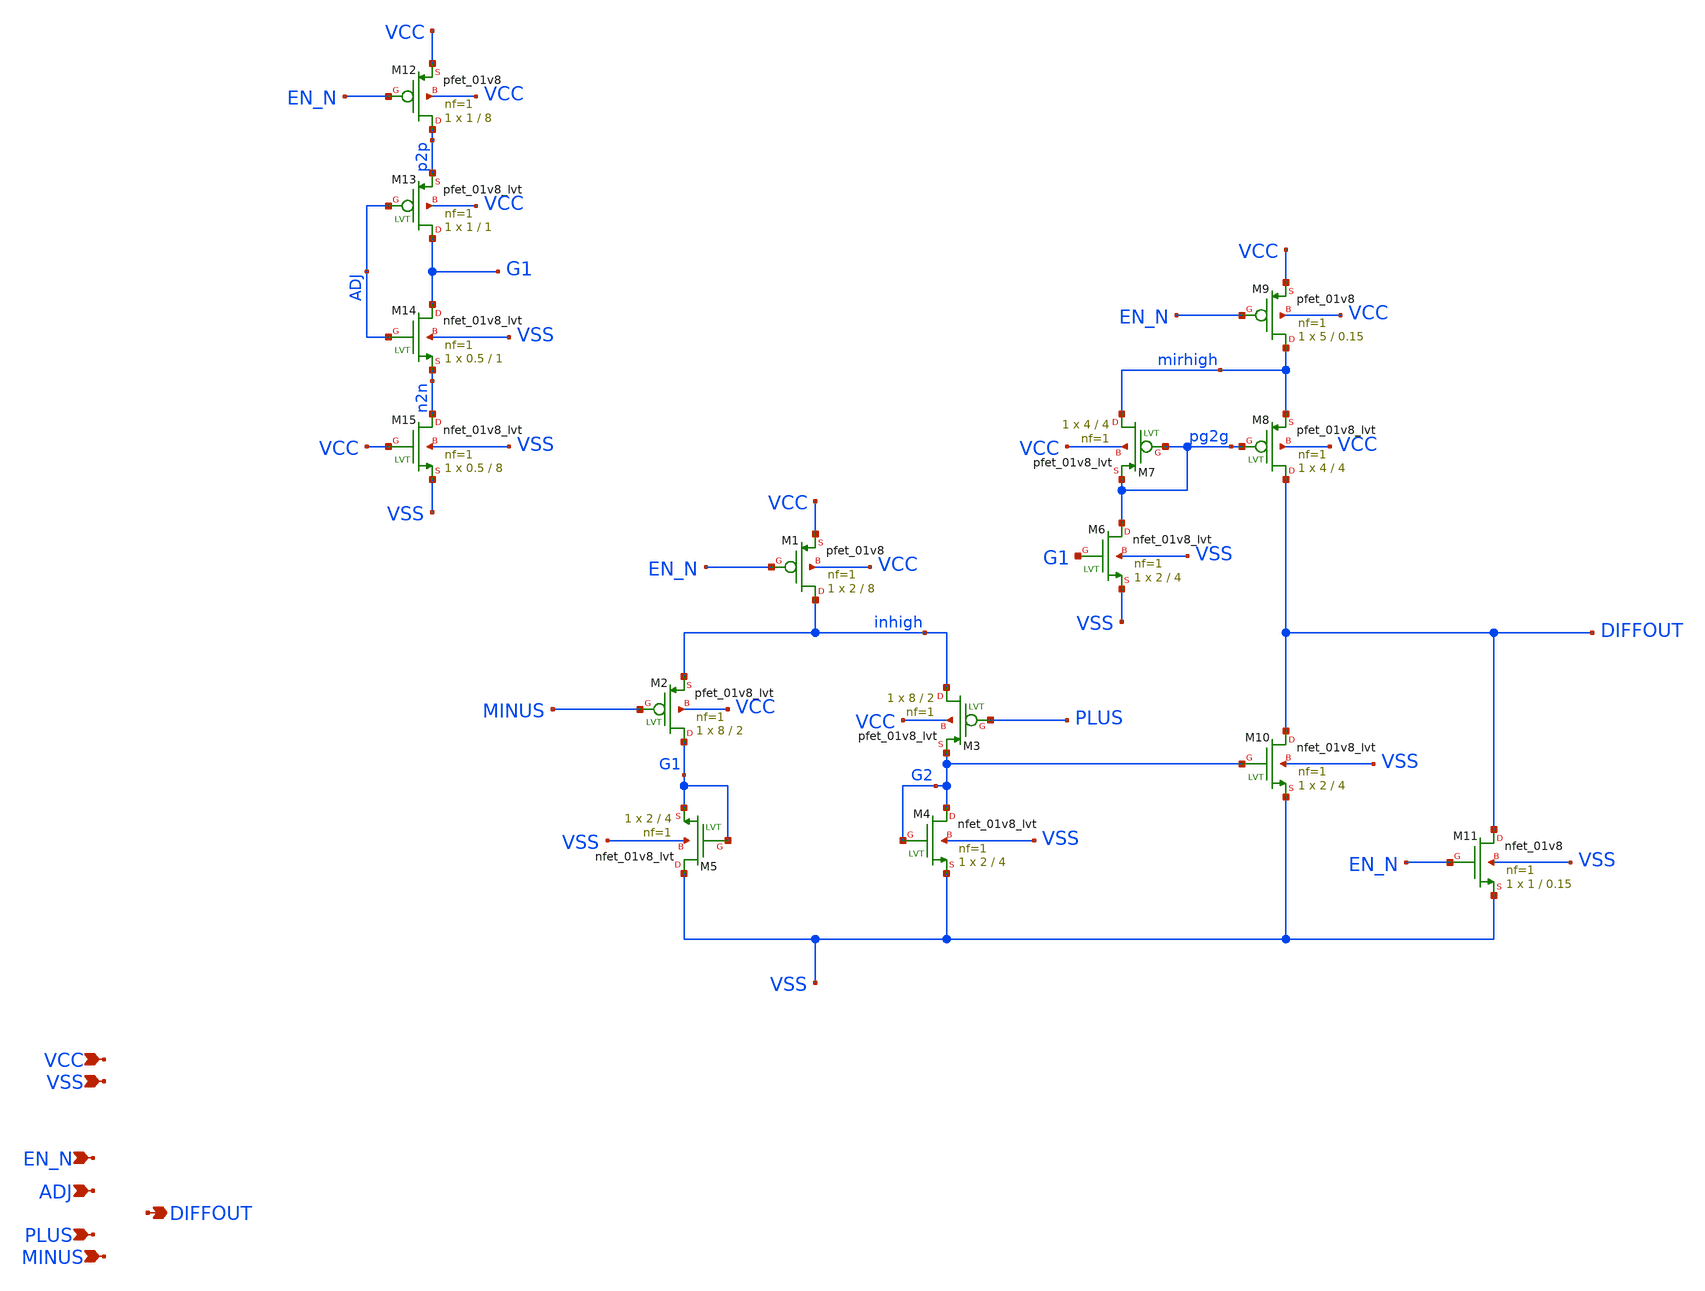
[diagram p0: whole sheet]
** sch_path: xschem/comparator_stefan.sch
**.subckt comparator_stefan PLUS MINUS VCC VSS EN_N ADJ DIFFOUT
*.ipin PLUS
*.ipin MINUS
*.ipin VCC
*.ipin VSS
*.ipin EN_N
*.ipin ADJ
*.opin DIFFOUT
XM1 inhigh EN_N VCC VCC sky130_fd_pr__pfet_01v8 L=8 W=2 nf=1 ad='int((nf+1)/2) * W/nf * 0.29' as='int((nf+2)/2) * W/nf * 0.29'
+ pd='2*int((nf+1)/2) * (W/nf + 0.29)' ps='2*int((nf+2)/2) * (W/nf + 0.29)' nrd='0.29 / W' nrs='0.29 / W'
+ sa=0 sb=0 sd=0 mult=1 m=1
XM2 G1 MINUS inhigh VCC sky130_fd_pr__pfet_01v8_lvt L=2 W=8 nf=1 ad='int((nf+1)/2) * W/nf * 0.29' as='int((nf+2)/2) * W/nf * 0.29'
+ pd='2*int((nf+1)/2) * (W/nf + 0.29)' ps='2*int((nf+2)/2) * (W/nf + 0.29)' nrd='0.29 / W' nrs='0.29 / W'
+ sa=0 sb=0 sd=0 mult=1 m=1
XM3 inhigh PLUS G2 VCC sky130_fd_pr__pfet_01v8_lvt L=2 W=8 nf=1 ad='int((nf+1)/2) * W/nf * 0.29' as='int((nf+2)/2) * W/nf * 0.29'
+ pd='2*int((nf+1)/2) * (W/nf + 0.29)' ps='2*int((nf+2)/2) * (W/nf + 0.29)' nrd='0.29 / W' nrs='0.29 / W'
+ sa=0 sb=0 sd=0 mult=1 m=1
XM4 G2 G2 VSS VSS sky130_fd_pr__nfet_01v8_lvt L=4 W=2 nf=1 ad='int((nf+1)/2) * W/nf * 0.29' as='int((nf+2)/2) * W/nf * 0.29'
+ pd='2*int((nf+1)/2) * (W/nf + 0.29)' ps='2*int((nf+2)/2) * (W/nf + 0.29)' nrd='0.29 / W' nrs='0.29 / W'
+ sa=0 sb=0 sd=0 mult=1 m=1
XM5 VSS G1 G1 VSS sky130_fd_pr__nfet_01v8_lvt L=4 W=2 nf=1 ad='int((nf+1)/2) * W/nf * 0.29' as='int((nf+2)/2) * W/nf * 0.29'
+ pd='2*int((nf+1)/2) * (W/nf + 0.29)' ps='2*int((nf+2)/2) * (W/nf + 0.29)' nrd='0.29 / W' nrs='0.29 / W'
+ sa=0 sb=0 sd=0 mult=1 m=1
XM6 pg2g G1 VSS VSS sky130_fd_pr__nfet_01v8_lvt L=4 W=2 nf=1 ad='int((nf+1)/2) * W/nf * 0.29' as='int((nf+2)/2) * W/nf * 0.29'
+ pd='2*int((nf+1)/2) * (W/nf + 0.29)' ps='2*int((nf+2)/2) * (W/nf + 0.29)' nrd='0.29 / W' nrs='0.29 / W'
+ sa=0 sb=0 sd=0 mult=1 m=1
XM7 mirhigh pg2g pg2g VCC sky130_fd_pr__pfet_01v8_lvt L=4 W=4 nf=1 ad='int((nf+1)/2) * W/nf * 0.29' as='int((nf+2)/2) * W/nf * 0.29'
+ pd='2*int((nf+1)/2) * (W/nf + 0.29)' ps='2*int((nf+2)/2) * (W/nf + 0.29)' nrd='0.29 / W' nrs='0.29 / W'
+ sa=0 sb=0 sd=0 mult=1 m=1
XM8 DIFFOUT pg2g mirhigh VCC sky130_fd_pr__pfet_01v8_lvt L=4 W=4 nf=1 ad='int((nf+1)/2) * W/nf * 0.29'
+ as='int((nf+2)/2) * W/nf * 0.29' pd='2*int((nf+1)/2) * (W/nf + 0.29)' ps='2*int((nf+2)/2) * (W/nf + 0.29)'
+ nrd='0.29 / W' nrs='0.29 / W' sa=0 sb=0 sd=0 mult=1 m=1
XM9 mirhigh EN_N VCC VCC sky130_fd_pr__pfet_01v8 L=0.15 W=5 nf=1 ad='int((nf+1)/2) * W/nf * 0.29' as='int((nf+2)/2) * W/nf * 0.29'
+ pd='2*int((nf+1)/2) * (W/nf + 0.29)' ps='2*int((nf+2)/2) * (W/nf + 0.29)' nrd='0.29 / W' nrs='0.29 / W'
+ sa=0 sb=0 sd=0 mult=1 m=1
XM10 DIFFOUT G2 VSS VSS sky130_fd_pr__nfet_01v8_lvt L=4 W=2 nf=1 ad='int((nf+1)/2) * W/nf * 0.29' as='int((nf+2)/2) * W/nf * 0.29'
+ pd='2*int((nf+1)/2) * (W/nf + 0.29)' ps='2*int((nf+2)/2) * (W/nf + 0.29)' nrd='0.29 / W' nrs='0.29 / W'
+ sa=0 sb=0 sd=0 mult=1 m=1
XM11 DIFFOUT EN_N VSS VSS sky130_fd_pr__nfet_01v8 L=0.15 W=1 nf=1 ad='int((nf+1)/2) * W/nf * 0.29' as='int((nf+2)/2) * W/nf * 0.29'
+ pd='2*int((nf+1)/2) * (W/nf + 0.29)' ps='2*int((nf+2)/2) * (W/nf + 0.29)' nrd='0.29 / W' nrs='0.29 / W'
+ sa=0 sb=0 sd=0 mult=1 m=1
XM12 p2p EN_N VCC VCC sky130_fd_pr__pfet_01v8 L=8 W=1 nf=1 ad='int((nf+1)/2) * W/nf * 0.29' as='int((nf+2)/2) * W/nf * 0.29'
+ pd='2*int((nf+1)/2) * (W/nf + 0.29)' ps='2*int((nf+2)/2) * (W/nf + 0.29)' nrd='0.29 / W' nrs='0.29 / W'
+ sa=0 sb=0 sd=0 mult=1 m=1
XM13 G1 ADJ p2p VCC sky130_fd_pr__pfet_01v8_lvt L=1 W=1 nf=1 ad='int((nf+1)/2) * W/nf * 0.29' as='int((nf+2)/2) * W/nf * 0.29'
+ pd='2*int((nf+1)/2) * (W/nf + 0.29)' ps='2*int((nf+2)/2) * (W/nf + 0.29)' nrd='0.29 / W' nrs='0.29 / W'
+ sa=0 sb=0 sd=0 mult=1 m=1
XM14 G1 ADJ n2n VSS sky130_fd_pr__nfet_01v8_lvt L=1 W=0.5 nf=1 ad='int((nf+1)/2) * W/nf * 0.29' as='int((nf+2)/2) * W/nf * 0.29'
+ pd='2*int((nf+1)/2) * (W/nf + 0.29)' ps='2*int((nf+2)/2) * (W/nf + 0.29)' nrd='0.29 / W' nrs='0.29 / W'
+ sa=0 sb=0 sd=0 mult=1 m=1
XM15 n2n VCC VSS VSS sky130_fd_pr__nfet_01v8_lvt L=8 W=0.5 nf=1 ad='int((nf+1)/2) * W/nf * 0.29' as='int((nf+2)/2) * W/nf * 0.29'
+ pd='2*int((nf+1)/2) * (W/nf + 0.29)' ps='2*int((nf+2)/2) * (W/nf + 0.29)' nrd='0.29 / W' nrs='0.29 / W'
+ sa=0 sb=0 sd=0 mult=1 m=1
**.ends
.end
